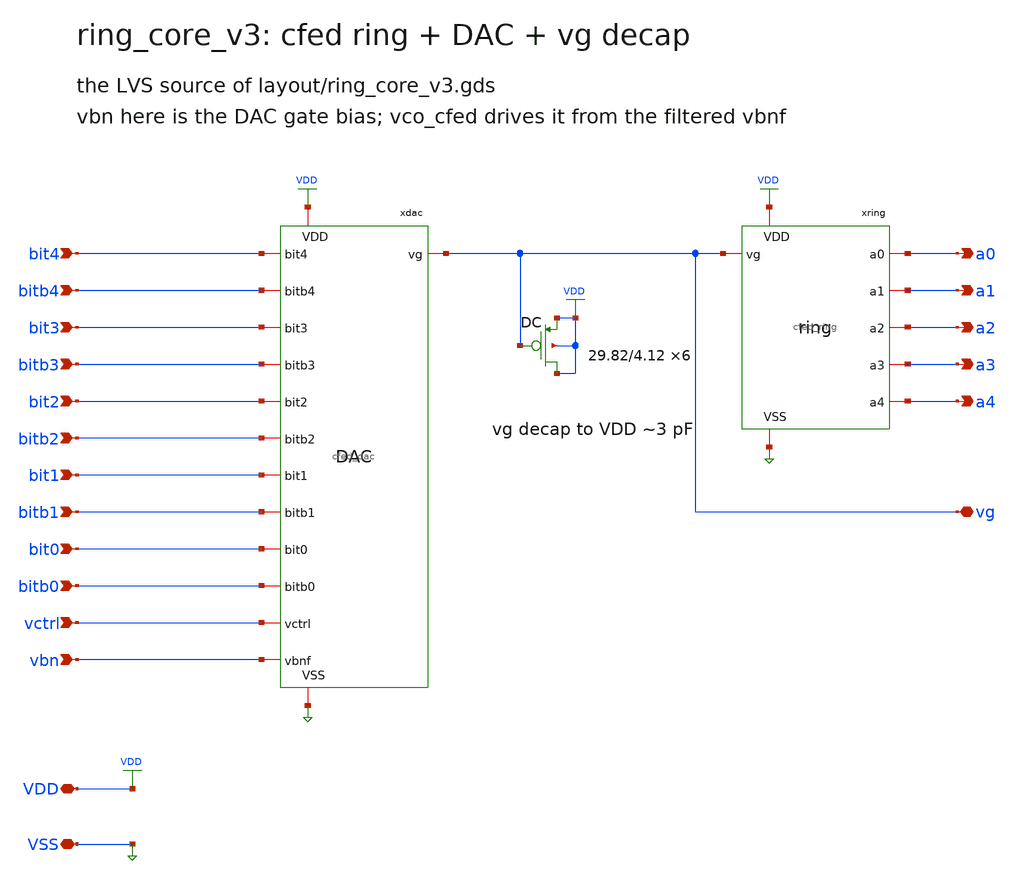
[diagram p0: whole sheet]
** sch_path: xschem/ring_core_v3.sch
**.subckt ring_core_v3 VDD VSS vbn vctrl bit0 bit1 bit2 bit3 bit4 bitb0 bitb1 bitb2 bitb3 bitb4 vg
*+ a0 a1 a2 a3 a4
*.iopin VDD
*.iopin VSS
*.ipin vbn
*.ipin vctrl
*.ipin bit0
*.ipin bit1
*.ipin bit2
*.ipin bit3
*.ipin bit4
*.ipin bitb0
*.ipin bitb1
*.ipin bitb2
*.ipin bitb3
*.ipin bitb4
*.iopin vg
*.opin a0
*.opin a1
*.opin a2
*.opin a3
*.opin a4
xdac vg vbn vctrl bit0 bit1 bit2 bit3 bit4 bitb0 bitb1 bitb2 bitb3 bitb4 VDD VSS cfed_dac
xring VDD vg VSS a0 a1 a2 a3 a4 cfed_ring
XDC VDD vg VDD VDD pfet_03v3 L=4.12u W=29.82u nf=1 ad=0 as=0 pd=0 ps=0 nrd=0 nrs=0 sa=0 sb=0 sd=0
+ m=6
**.ends

* expanding   symbol:  cfed_dac.sym # of pins=15
** sym_path: xschem/cfed_dac.sym
** sch_path: xschem/cfed_dac.sch
.subckt cfed_dac vg vbnf vctrl bit0 bit1 bit2 bit3 bit4 bitb0 bitb1 bitb2 bitb3 bitb4 VDD VSS
*.iopin vg
*.ipin vbnf
*.ipin vctrl
*.ipin bit0
*.ipin bit1
*.ipin bit2
*.ipin bit3
*.ipin bit4
*.ipin bitb0
*.ipin bitb1
*.ipin bitb2
*.ipin bitb3
*.ipin bitb4
*.iopin VDD
*.iopin VSS
XFFC vg vctrl VSS VSS nfet_03v3 L=21.333333333333332u W=1.2u nf=1 ad=0.6p as=0.6p pd=3.4u ps=3.4u
+ nrd=0 nrs=0 sa=0 sb=0 sd=0 m=1
XFC vg vbnf VSS VSS nfet_03v3 L=5.333333333333333u W=1.2u nf=1 ad=0.6p as=0.6p pd=3.4u ps=3.4u nrd=0
+ nrs=0 sa=0 sb=0 sd=0 m=6
XFC_0 vg net1 VSS VSS nfet_03v3 L=5.333333333333333u W=1.2u nf=1 ad=0.6p as=0.6p pd=3.4u ps=3.4u
+ nrd=0 nrs=0 sa=0 sb=0 sd=0 m=1
XFC_1 vg net2 VSS VSS nfet_03v3 L=5.333333333333333u W=1.2u nf=1 ad=0.6p as=0.6p pd=3.4u ps=3.4u
+ nrd=0 nrs=0 sa=0 sb=0 sd=0 m=2
XFC_2 vg net3 VSS VSS nfet_03v3 L=5.333333333333333u W=1.2u nf=1 ad=0.6p as=0.6p pd=3.4u ps=3.4u
+ nrd=0 nrs=0 sa=0 sb=0 sd=0 m=4
XFC_3 vg net4 VSS VSS nfet_03v3 L=5.333333333333333u W=1.2u nf=1 ad=0.6p as=0.6p pd=3.4u ps=3.4u
+ nrd=0 nrs=0 sa=0 sb=0 sd=0 m=8
XFC_4 vg net5 VSS VSS nfet_03v3 L=5.333333333333333u W=1.2u nf=1 ad=0.6p as=0.6p pd=3.4u ps=3.4u
+ nrd=0 nrs=0 sa=0 sb=0 sd=0 m=16
XTN0 net1 bit0 vbnf VSS nfet_03v3 L=0.28u W=2.0u nf=1 ad=1.0p as=1.0p pd=5.0u ps=5.0u nrd=0 nrs=0
+ sa=0 sb=0 sd=0 m=1
XTP0 net1 bitb0 vbnf VDD pfet_03v3 L=0.28u W=5.0u nf=1 ad=2.5p as=2.5p pd=11.0u ps=11.0u nrd=0 nrs=0
+ sa=0 sb=0 sd=0 m=1
XTD0 net1 bitb0 VSS VSS nfet_03v3 L=0.28u W=1.0u nf=1 ad=0.5p as=0.5p pd=3.0u ps=3.0u nrd=0 nrs=0
+ sa=0 sb=0 sd=0 m=1
XTN1 net2 bit1 vbnf VSS nfet_03v3 L=0.28u W=2.0u nf=1 ad=1.0p as=1.0p pd=5.0u ps=5.0u nrd=0 nrs=0
+ sa=0 sb=0 sd=0 m=1
XTP1 net2 bitb1 vbnf VDD pfet_03v3 L=0.28u W=5.0u nf=1 ad=2.5p as=2.5p pd=11.0u ps=11.0u nrd=0 nrs=0
+ sa=0 sb=0 sd=0 m=1
XTD1 net2 bitb1 VSS VSS nfet_03v3 L=0.28u W=1.0u nf=1 ad=0.5p as=0.5p pd=3.0u ps=3.0u nrd=0 nrs=0
+ sa=0 sb=0 sd=0 m=1
XTN2 net3 bit2 vbnf VSS nfet_03v3 L=0.28u W=2.0u nf=1 ad=1.0p as=1.0p pd=5.0u ps=5.0u nrd=0 nrs=0
+ sa=0 sb=0 sd=0 m=1
XTP2 net3 bitb2 vbnf VDD pfet_03v3 L=0.28u W=5.0u nf=1 ad=2.5p as=2.5p pd=11.0u ps=11.0u nrd=0 nrs=0
+ sa=0 sb=0 sd=0 m=1
XTD2 net3 bitb2 VSS VSS nfet_03v3 L=0.28u W=1.0u nf=1 ad=0.5p as=0.5p pd=3.0u ps=3.0u nrd=0 nrs=0
+ sa=0 sb=0 sd=0 m=1
XTN3 net4 bit3 vbnf VSS nfet_03v3 L=0.28u W=2.0u nf=1 ad=1.0p as=1.0p pd=5.0u ps=5.0u nrd=0 nrs=0
+ sa=0 sb=0 sd=0 m=1
XTP3 net4 bitb3 vbnf VDD pfet_03v3 L=0.28u W=5.0u nf=1 ad=2.5p as=2.5p pd=11.0u ps=11.0u nrd=0 nrs=0
+ sa=0 sb=0 sd=0 m=1
XTD3 net4 bitb3 VSS VSS nfet_03v3 L=0.28u W=1.0u nf=1 ad=0.5p as=0.5p pd=3.0u ps=3.0u nrd=0 nrs=0
+ sa=0 sb=0 sd=0 m=1
XTN4 net5 bit4 vbnf VSS nfet_03v3 L=0.28u W=2.0u nf=1 ad=1.0p as=1.0p pd=5.0u ps=5.0u nrd=0 nrs=0
+ sa=0 sb=0 sd=0 m=1
XTP4 net5 bitb4 vbnf VDD pfet_03v3 L=0.28u W=5.0u nf=1 ad=2.5p as=2.5p pd=11.0u ps=11.0u nrd=0 nrs=0
+ sa=0 sb=0 sd=0 m=1
XTD4 net5 bitb4 VSS VSS nfet_03v3 L=0.28u W=1.0u nf=1 ad=0.5p as=0.5p pd=3.0u ps=3.0u nrd=0 nrs=0
+ sa=0 sb=0 sd=0 m=1
.ends


* expanding   symbol:  cfed_ring.sym # of pins=8
** sym_path: xschem/cfed_ring.sym
** sch_path: xschem/cfed_ring.sch
.subckt cfed_ring VDD vg VSS a0 a1 a2 a3 a4
*.iopin VDD
*.iopin vg
*.iopin VSS
*.opin a0
*.opin a1
*.opin a2
*.opin a3
*.opin a4
XP0 a1 a0 VDD VDD pfet_03v3 L=0.28u W=5.0u nf=1 ad=2.5p as=2.5p pd=11.0u ps=11.0u nrd=0 nrs=0 sa=0
+ sb=0 sd=0 m=1
XN0 a1 a0 vg VSS nfet_03v3 L=0.28u W=2.0u nf=1 ad=1.0p as=1.0p pd=5.0u ps=5.0u nrd=0 nrs=0 sa=0 sb=0
+ sd=0 m=1
XP1 a2 a1 VDD VDD pfet_03v3 L=0.28u W=5.0u nf=1 ad=2.5p as=2.5p pd=11.0u ps=11.0u nrd=0 nrs=0 sa=0
+ sb=0 sd=0 m=1
XN1 a2 a1 vg VSS nfet_03v3 L=0.28u W=2.0u nf=1 ad=1.0p as=1.0p pd=5.0u ps=5.0u nrd=0 nrs=0 sa=0 sb=0
+ sd=0 m=1
XP2 a3 a2 VDD VDD pfet_03v3 L=0.28u W=5.0u nf=1 ad=2.5p as=2.5p pd=11.0u ps=11.0u nrd=0 nrs=0 sa=0
+ sb=0 sd=0 m=1
XN2 a3 a2 vg VSS nfet_03v3 L=0.28u W=2.0u nf=1 ad=1.0p as=1.0p pd=5.0u ps=5.0u nrd=0 nrs=0 sa=0 sb=0
+ sd=0 m=1
XP3 a4 a3 VDD VDD pfet_03v3 L=0.28u W=5.0u nf=1 ad=2.5p as=2.5p pd=11.0u ps=11.0u nrd=0 nrs=0 sa=0
+ sb=0 sd=0 m=1
XN3 a4 a3 vg VSS nfet_03v3 L=0.28u W=2.0u nf=1 ad=1.0p as=1.0p pd=5.0u ps=5.0u nrd=0 nrs=0 sa=0 sb=0
+ sd=0 m=1
XP4 a0 a4 VDD VDD pfet_03v3 L=0.28u W=5.0u nf=1 ad=2.5p as=2.5p pd=11.0u ps=11.0u nrd=0 nrs=0 sa=0
+ sb=0 sd=0 m=1
XN4 a0 a4 vg VSS nfet_03v3 L=0.28u W=2.0u nf=1 ad=1.0p as=1.0p pd=5.0u ps=5.0u nrd=0 nrs=0 sa=0 sb=0
+ sd=0 m=1
.ends

.end
